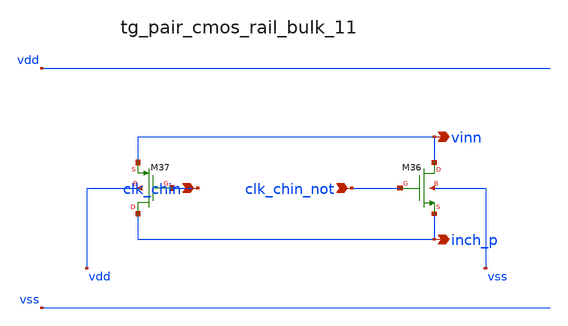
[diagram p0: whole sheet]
** sch_path: analog-db/raw/ia_003_fan_chopper_pf/hier/blocks/tg_pair_cmos_rail_bulk_11.sch
**.subckt tg_pair_cmos_rail_bulk_11 clk_chin clk_chin_not vinn inch_p
*.ipin clk_chin
*.ipin clk_chin_not
*.opin vinn
*.opin inch_p
XM36 vinn clk_chin_not inch_p vss sg13_lv_nmos w=x_dut_xm36_w l=x_dut_xm36_l ng=1 m=x_dut_xm36_m
XM37 inch_p clk_chin vinn vdd sg13_lv_pmos w=x_dut_xm37_w l=x_dut_xm37_l ng=1 m=x_dut_xm37_m
**.ends
.end
